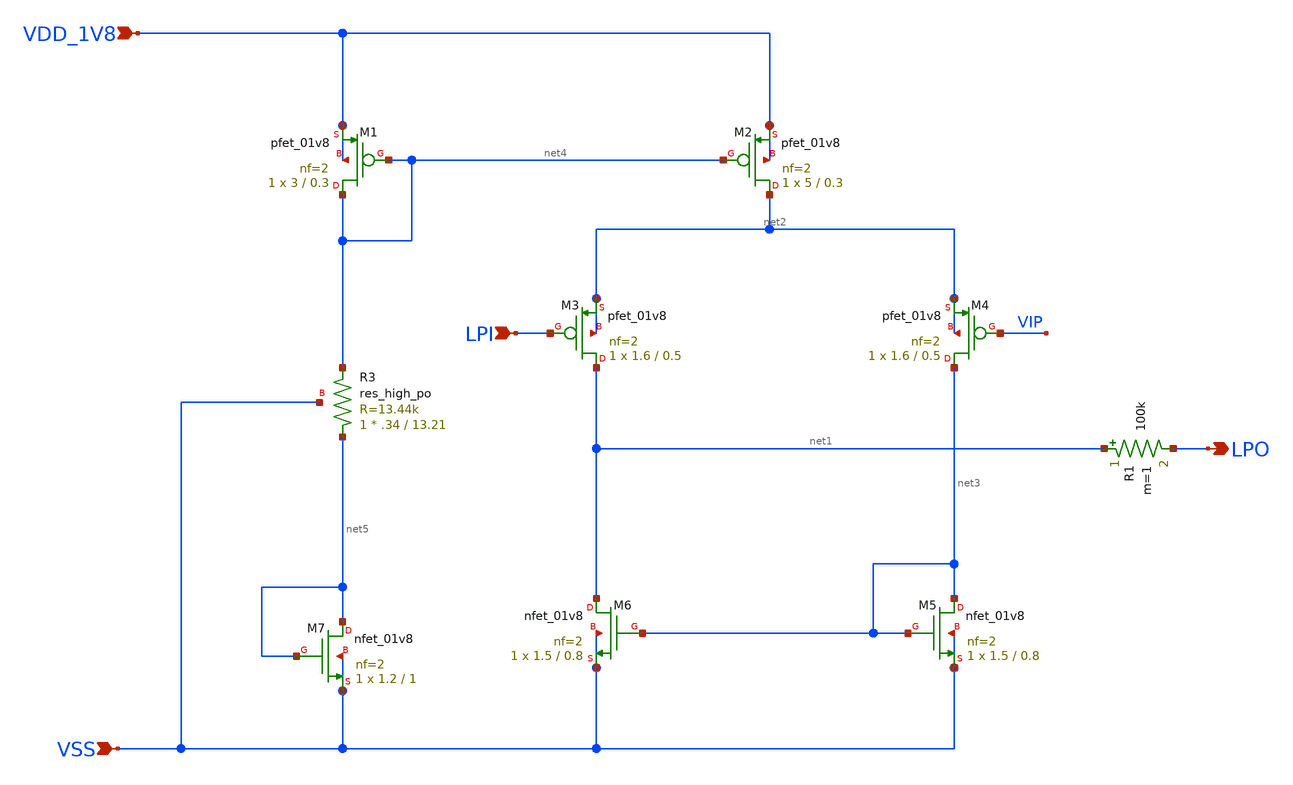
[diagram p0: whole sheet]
** sch_path: design/OTA_SKY130NM/OTA.sch
**.subckt OTA VSS VDD_1V8 LPO LPI
*.ipin VSS
*.ipin VDD_1V8
*.opin LPO
*.ipin LPI
R1 net1 LPO 100k m=1
XM1 net4 net4 VDD_1V8 VDD_1V8 sky130_fd_pr__pfet_01v8 L=0.3 W=3 nf=2 ad='int((nf+1)/2) * W/nf * 0.29'
+ as='int((nf+2)/2) * W/nf * 0.29' pd='2*int((nf+1)/2) * (W/nf + 0.29)' ps='2*int((nf+2)/2) * (W/nf + 0.29)'
+ nrd='0.29 / W' nrs='0.29 / W' sa=0 sb=0 sd=0 mult=1 m=1
XM2 net2 net4 VDD_1V8 VDD_1V8 sky130_fd_pr__pfet_01v8 L=0.3 W=5 nf=2 ad='int((nf+1)/2) * W/nf * 0.29'
+ as='int((nf+2)/2) * W/nf * 0.29' pd='2*int((nf+1)/2) * (W/nf + 0.29)' ps='2*int((nf+2)/2) * (W/nf + 0.29)'
+ nrd='0.29 / W' nrs='0.29 / W' sa=0 sb=0 sd=0 mult=1 m=1
XM3 net1 LPI net2 net2 sky130_fd_pr__pfet_01v8 L=0.5 W=1.6 nf=2 ad='int((nf+1)/2) * W/nf * 0.29' as='int((nf+2)/2) * W/nf * 0.29'
+ pd='2*int((nf+1)/2) * (W/nf + 0.29)' ps='2*int((nf+2)/2) * (W/nf + 0.29)' nrd='0.29 / W' nrs='0.29 / W'
+ sa=0 sb=0 sd=0 mult=1 m=1
XM4 net3 VIP net2 net2 sky130_fd_pr__pfet_01v8 L=0.5 W=1.6 nf=2 ad='int((nf+1)/2) * W/nf * 0.29' as='int((nf+2)/2) * W/nf * 0.29'
+ pd='2*int((nf+1)/2) * (W/nf + 0.29)' ps='2*int((nf+2)/2) * (W/nf + 0.29)' nrd='0.29 / W' nrs='0.29 / W'
+ sa=0 sb=0 sd=0 mult=1 m=1
XM5 net3 net3 VSS VSS sky130_fd_pr__nfet_01v8 L=0.8 W=1.5 nf=2 ad='int((nf+1)/2) * W/nf * 0.29' as='int((nf+2)/2) * W/nf * 0.29'
+ pd='2*int((nf+1)/2) * (W/nf + 0.29)' ps='2*int((nf+2)/2) * (W/nf + 0.29)' nrd='0.29 / W' nrs='0.29 / W'
+ sa=0 sb=0 sd=0 mult=1 m=1
XM6 net1 net3 VSS VSS sky130_fd_pr__nfet_01v8 L=0.8 W=1.5 nf=2 ad='int((nf+1)/2) * W/nf * 0.29' as='int((nf+2)/2) * W/nf * 0.29'
+ pd='2*int((nf+1)/2) * (W/nf + 0.29)' ps='2*int((nf+2)/2) * (W/nf + 0.29)' nrd='0.29 / W' nrs='0.29 / W'
+ sa=0 sb=0 sd=0 mult=1 m=1
XM7 net5 net5 VSS VSS sky130_fd_pr__nfet_01v8 L=1 W=1.2 nf=2 ad='int((nf+1)/2) * W/nf * 0.29' as='int((nf+2)/2) * W/nf * 0.29'
+ pd='2*int((nf+1)/2) * (W/nf + 0.29)' ps='2*int((nf+2)/2) * (W/nf + 0.29)' nrd='0.29 / W' nrs='0.29 / W'
+ sa=0 sb=0 sd=0 mult=1 m=1
XR3 net5 net4 VSS sky130_fd_pr__res_high_po W=.34 L=13.21 mult=1 m=1
**.ends
.end
